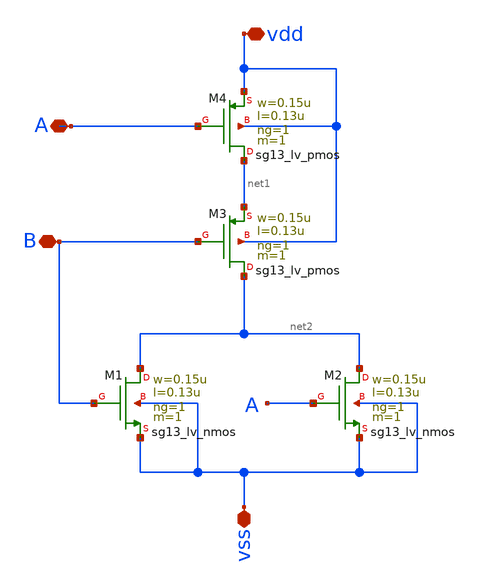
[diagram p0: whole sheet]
** sch_path: design/blocks/nor2/schematic/untitled.sch
**.subckt untitled vdd A B vss
*.iopin vdd
*.iopin A
*.iopin B
*.iopin vss
XM1 net2 B vss vss sg13_lv_nmos w=0.15u l=0.13u ng=1 m=1 mm_ok=1
XM2 net2 A vss vss sg13_lv_nmos w=0.15u l=0.13u ng=1 m=1 mm_ok=1
XM3 net2 B net1 vdd sg13_lv_pmos w=0.15u l=0.13u ng=1 m=1 mm_ok=1
XM4 net1 A vdd vdd sg13_lv_pmos w=0.15u l=0.13u ng=1 m=1 mm_ok=1
**.ends
.end
